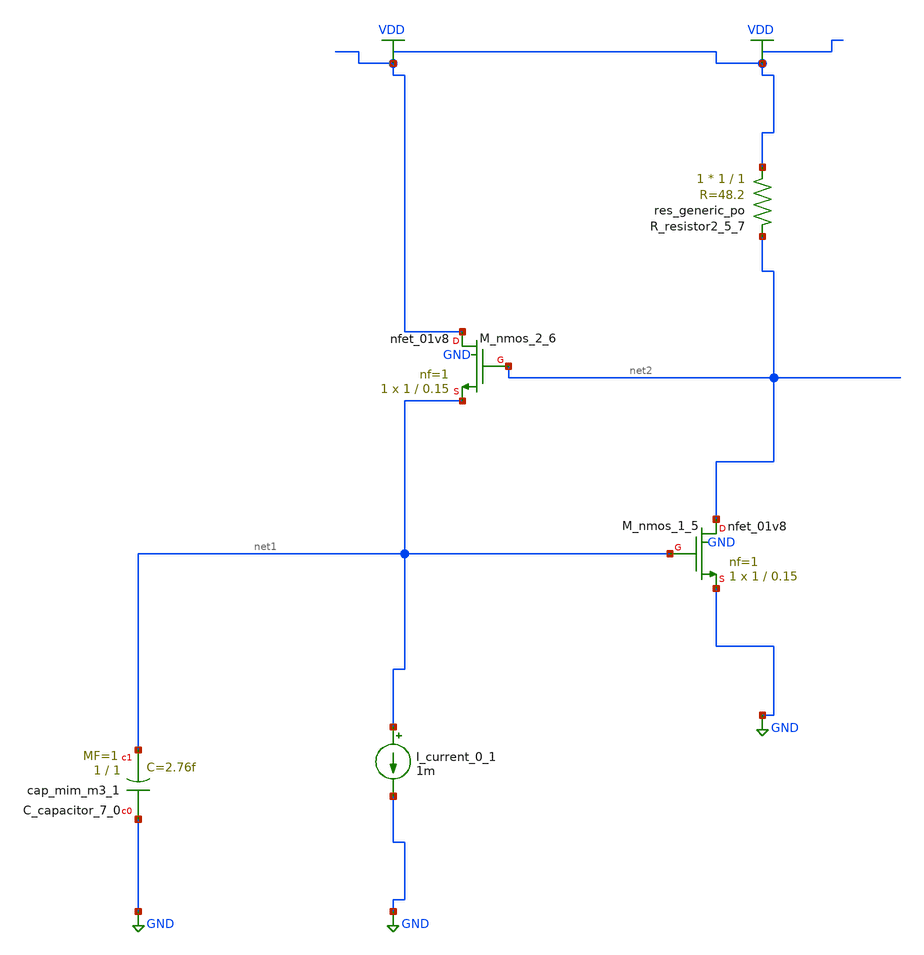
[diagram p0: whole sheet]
** sch_path: schematics/AMSNet/425.sch
**.subckt 425
XC_capacitor_7_0 GND net1 sky130_fd_pr__cap_mim_m3_1 W=1 L=1 MF=1 m=1
I_current_0_1 net1 GND 1m
XM_nmos_1_5 net2 net1 GND GND sky130_fd_pr__nfet_01v8 L=0.15 W=1 nf=1 ad='int((1 + 1)/2) * 1 / 1 * 0.29'
+ as='int((1 + 2)/2) * 1 / 1 * 0.29' pd='2*int((1 + 1)/2) * (1 / 1 + 0.29)' ps='2*int((1 + 2)/2) * (1 / 1 + 0.29)'
+ nrd='0.29 / 1 ' nrs='0.29 / 1 ' sa=0 sb=0 sd=0 mult=1 m=1
XM_nmos_2_6 VDD net2 net1 GND sky130_fd_pr__nfet_01v8 L=0.15 W=1 nf=1 ad='int((1 + 1)/2) * 1 / 1 * 0.29'
+ as='int((1 + 2)/2) * 1 / 1 * 0.29' pd='2*int((1 + 1)/2) * (1 / 1 + 0.29)' ps='2*int((1 + 2)/2) * (1 / 1 + 0.29)'
+ nrd='0.29 / 1 ' nrs='0.29 / 1 ' sa=0 sb=0 sd=0 mult=1 m=1
XR_resistor2_5_7 VDD net2 sky130_fd_pr__res_generic_po W=1 L=1 m=1
**.ends
.GLOBAL GND
.GLOBAL VDD
.end
